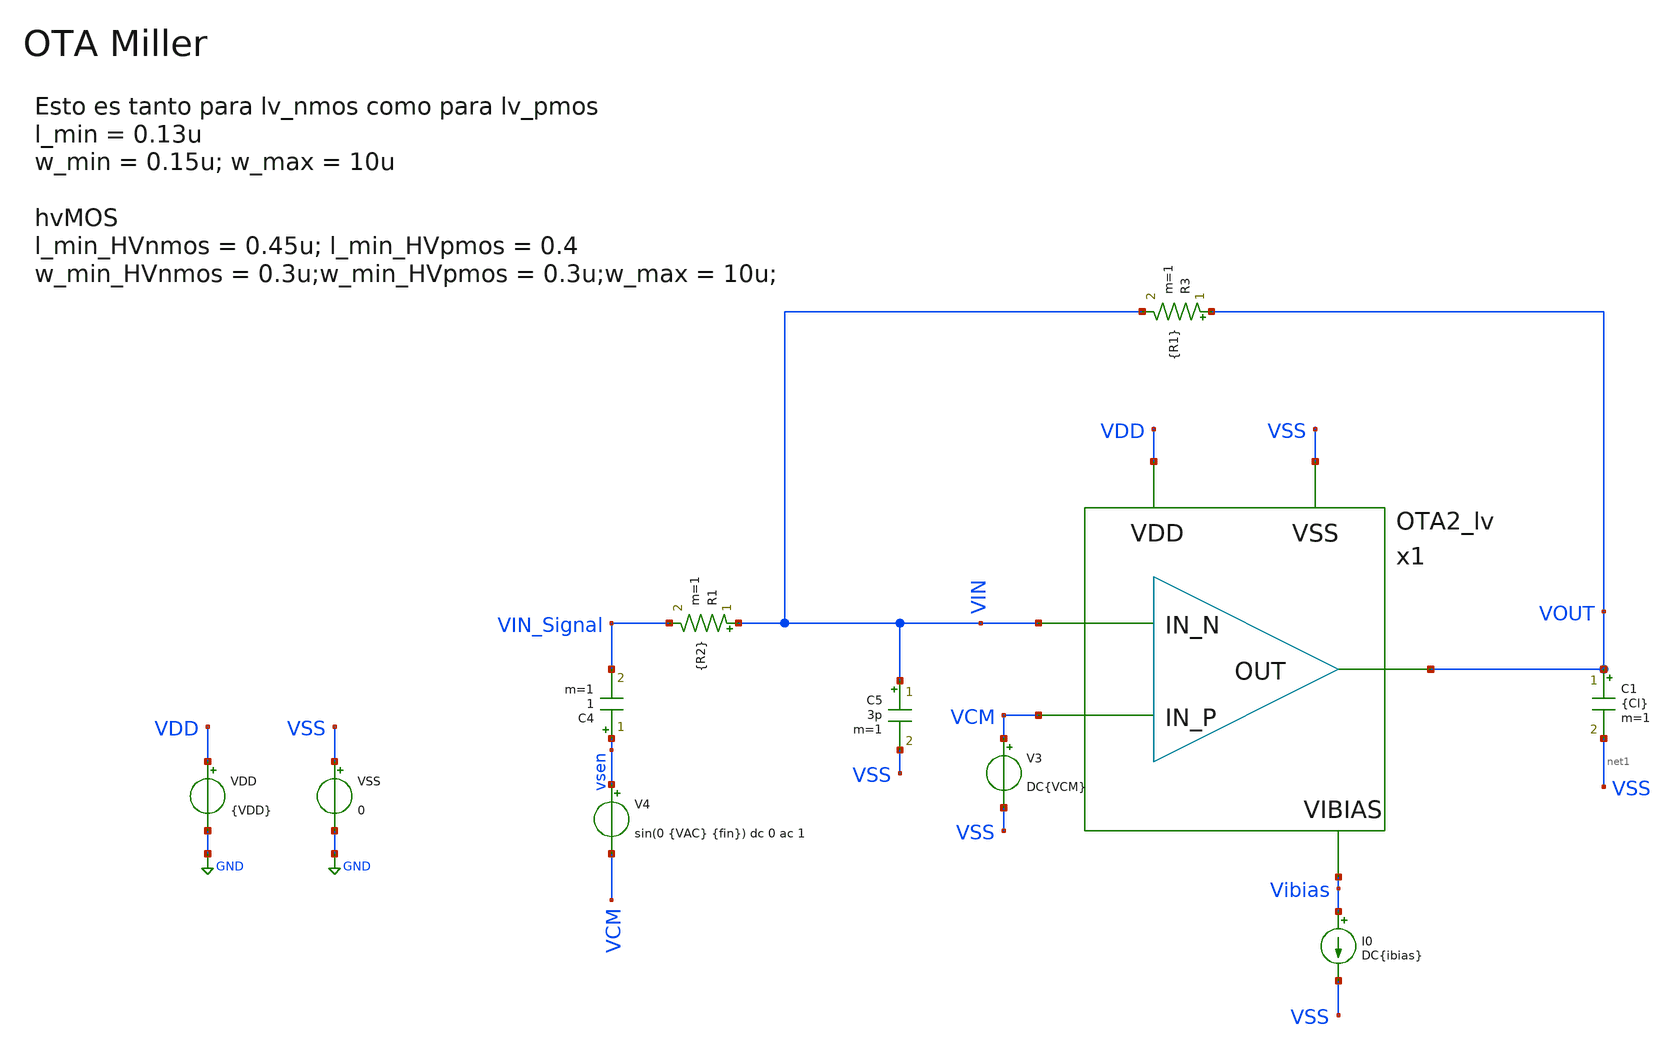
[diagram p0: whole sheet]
** sch_path: xschem/Ayudantias/Ayudantia_2/TB_OTA2_CL.sch
**.subckt TB_OTA2_CL
VDD VDD GND {VDD}
I0 Vibias VSS DC{ibias}
R3 VOUT VIN {R1} m=1
V3 VCM VSS DC{VCM}
VSS VSS GND 0
C5 VIN VSS 3p m=1
R1 VIN VIN_Signal {R2} m=1
C1 VOUT net1 {Cl} m=1
V4 vsen VCM sin(0 {VAC} {fin}) dc 0 ac 1
C4 vsen VIN_Signal 1 m=1
x1 VIN VCM VOUT VDD VSS Vibias OTA2_lv
**** begin user architecture code


*.param VDD = 3.3
.param VDD = 1.2
.param VCM = 0.6
.param Ibias = 100u
.param Pi = 3.14159265
.param fo = 60Meg
.param wo = 2*Pi*fo
.csparam wo = {wo}

.param VAC = 10m
*.param VAC  = 30m
*.param fin  = 9.765625e5
.param fin  = 0.8e5
.param T = 1/fin

.param R1 = 100k
*.param R2 = R1/10
.param R2 = R1/30

*.ic v(Vo) = 0

* OP Parameters & Singals to save
.save all

*.option temp = 125
*.option temp = -40
.option temp = 27





.lib cornerMOShv.lib mos_tt
.lib cornerMOSlv.lib mos_tt
*.lib cornerMOShv.lib mos_ff
*.lib cornerMOSlv.lib mos_ff
*.lib cornerMOShv.lib mos_ss
*.lib cornerMOSlv.lib mos_ss
*.lib cornerMOShv.lib mos_sf
*.lib cornerMOSlv.lib mos_sf
*.lib cornerMOShv.lib mos_fs
*.lib cornerMOSlv.lib mos_fs

.include /opt/pdks/ihp-sg13g2/libs.ref/sg13g2_stdcell/spice/sg13g2_stdcell.spice
.lib $::SG13G2_MODELS/cornerRES.lib res_typ
.lib $::SG13G2_MODELS/cornerCAP.lib cap_typ
*.lib $::SG13G2_MODELS/diodes.lib




*.param SimTime = 10*T
*.tran 0.01u {SimTime} uic
*.save all v(vsen)
.control
reset
  set color0 = white
  tran 0.01u 110u
  setplot tran1
  plot v(vsen) v(VOUT)
.endc

.end





.control
  set color0 = white
  *IPD413
 ac dec 200 1 1000Meg
 settype decibel VOUT
 *setplot ac1

 let phase_val = (180/PI)*cph(VOUT)
 *let phase_margin_val = 180 + 180/PI*cph(VOUT)
 let phase_margin_val = 360 + 180/PI*cph(VOUT)
 settype phase phase_val
 meas ac PM find phase_margin_val when vdb(VOUT)=0
 *meas ac PM find phase_val when vdb(VOUT)=0
 meas ac GM find vdb(vout) when vp(vout)=0
 *meas ac GM2 find vdb(vout) when vp(vout)=-180
 meas ac GBW WHEN vdb(VOUT)=0
 meas ac DCG find vdb(vout) at=1
 let DCG_BW = {DCG} - 3
 meas ac BW WHEN vdb(VOUT)={DCG_BW}

 let Av = 10^(DCG/20)
 print Av

 plot vdb(VOUT)
 plot phase_val
 plot phase_val vdb(VOUT)


 *wrdata /foss/designs/IPD413_2023_HW3_git/Data/data_phaseOTA1.dat phase_val
 *wrdata /foss/designs/IPD413_2023_HW3_git/Data/data_VdbOTA1.dat vdb(out)

 reset
  *DACI
  *ac dec 100 1 10G
  *setplot ac1
  *meas ac GBW when vdb(vout)=0
  *meas ac DCG find vdb(vout) at=1
  *meas ac PM find vp(vout) when vdb(vout)=0
  *print PM*180/PI
  *meas ac GM find vdb(vout) when vp(vout)=0

  *plot vdb(vout)
  *plot {vp(vout)*180/PI}
  *plot vdb(vout) {vp(vout)*180/PI}
.endc


.end





.param VDD = 1.2
.param VCM = 0.6

.control
reset
  op
  setplot op1
  unset filetype
  * VM1
  let VsdM1 = v(x1.VA) - v(x1.VB)
  let VsgM1 = v(x1.VA) - v(VCM)
  let VthM1 = @n.x1.xm1.nsg13_lv_pmos[vth]
  let VovM1 = VsgM1 - VthM1
  let gmM1 = @n.x1.xm1.nsg13_lv_pmos[gm]
  let gdsM1 = @n.x1.xm1.nsg13_lv_pmos[gds]
  let RoM1 = 1/gdsM1
  * VM2
  let VsdM2 = v(x1.VA) - v(x1.VC)
  let VsgM2 = v(x1.VA) - v(VIN)
  let VthM2 = @n.x1.xm2.nsg13_lv_pmos[vth]
  let VovM2 = VsgM2 - VthM2
  let gmM2 = @n.x1.xm2.nsg13_lv_pmos[gm]
  let gdsM2 = @n.x1.xm2.nsg13_lv_pmos[gds]
  let RoM2 = 1/gdsM2
  * VM3
  let VdsM3 = v(x1.VB) - v(VSS)
  let VthM3 = @n.x1.xm3.nsg13_lv_nmos[vth]
  let gmM3 = @n.x1.xm3.nsg13_lv_nmos[gm]
  let gdsM3 = @n.x1.xm3.nsg13_lv_nmos[gds]
  let RoM3 = 1/gdsM3
  * VM4
  let VdsM4 = v(x1.VC) - v(VSS)
  let VgsM4 = v(x1.VB) - v(VSS)
  let VthM4 = @n.x1.xm4.nsg13_lv_nmos[vth]
  let VovM4 = VgsM4 - VthM4
  let gmM4 = @n.x1.xm4.nsg13_lv_nmos[gm]
  let gdsM4 = @n.x1.xm4.nsg13_lv_nmos[gds]
  let RoM4 = 1/gdsM4
  * VM5
  let VsdM5 = v(VDD) - v(VOUT)
  let VsgM5 = v(VDD) - v(Vibias)
  let VthM5 = @n.x1.xm5.nsg13_lv_pmos[vth]
  let VovM5 = VsgM5 - VthM5
  let gmM5 = @n.x1.xm5.nsg13_lv_pmos[gm]
  let gdsM5 = @n.x1.xm5.nsg13_lv_pmos[gds]
  let RoM5 = 1/gdsM5
  * VM6
  let VdsM6 = v(VOUT) - v(VSS)
  let VgsM6 = v(x1.VC) - v(VSS)
  let VthM6 = @n.x1.xm6.nsg13_lv_nmos[vth]
  let VovM6 = VgsM6 - VthM6
  let gmM6 = @n.x1.xm6.nsg13_lv_nmos[gm]
  let gdsM6 = @n.x1.xm6.nsg13_lv_nmos[gds]
  let CggM6 = @n.x1.xm6.nsg13_lv_nmos[cgg]
  let RoM6 = 1/gdsM6
  * VM7
  let VsdM7 = v(VDD) - v(x1.VA)
  let VsgM7 = v(VDD) - v(Vibias)
  let VthM7 = @n.x1.xm7.nsg13_lv_pmos[vth]
  let VovM7 = VsgM7 - VthM7
  let gmM7 = @n.x1.xm7.nsg13_lv_pmos[gm]
  let gdsM7 = @n.x1.xm7.nsg13_lv_pmos[gds]
  let RoM7 = 1/gdsM7
  * VM8
  let VsdM8 = v(VDD) - v(Vibias)
  let VthM8 = @n.x1.xm8.nsg13_lv_pmos[vth]
  let VovM8 = VsdM8 - VthM8
  let gmM8 = @n.x1.xm8.nsg13_lv_pmos[gm]
  let gdsM8 = @n.x1.xm8.nsg13_lv_pmos[gds]
  let RoM8 = 1/gdsM8
  * VMR
  let VdsMR = v(x1.VC) - v(x1.VsMR)
  let gdsMR = @n.x1.xm9.nsg13_lv_nmos[gds]
  let RoMR = 1/gdsMR

  let Cc2 = gmM2/{wo}
  let Rc = 1/gmM6

  let Av1 = gmM1/(gdsM2+gdsM4)
  let Av2 = gmM6/(gdsM5+gdsM6)
  let Av = Av1*Av2
  let BW = (gdsM2+gdsM4)/(2*pi*Av2*{Cc})
  *let w1 = 1/((gdsM2+gdsM4)*gmM6*(gdsM6+gdsM7)*{Cc})
  *let w22 = gmM6/(CggM6+{Cl})
  let w2 = gmM6/(({Cl})*(1+CggM6/{Cc}))
  let GBW = gmM1/(2*pi*{Cc})
  *let GBW2 = gmM1/{Cc}
  let DCG = 20*log10(Av)
  *let fnd = gmM6/(2*pi*{Cl})

  print Av1 Av2 Av DCG
  print BW GBW w2
  print Rc Cc2

  write TB_OTA2_CL.raw
.endc

.end




.param temp=27

.param m_M8 = 500
.param m_M7 = 40
.param m_M5 = 11000
.param w_M8 =0.5u
.param w_M7 =0.5u
.param w_M5 =0.5u
.param l_M875 = 1u

.param m_M12 = 40
.param w_M12 =0.3u
.param l_M12 = 0.3u

.param m_M34 = 1
.param w_M34 =0.15u
.param l_M34 = 0.5u

.param m_M6 = 10
.param w_M6 =10u
.param l_M6 = 0.13u

.param m_R = 1
.param w_R =0.15u
.param l_R = 0.13u

.param Cc = 0.1p
.param Cl = 20p
.csparam Cl = {Cl}
.csparam Cc = {Cc}






**** end user architecture code
**.ends

* expanding   symbol:
*+  /workspaces/usm-vlsi-tools/shared_xserver/simulations/Projects/IHP/IPD413_202501/xschem/Tareas/Tarea_2/OTA2_lv.sym # of pins=6
** sym_path: xschem/Ayudantias/Ayudantia_2/OTA2_lv.sym
** sch_path: xschem/Ayudantias/Ayudantia_2/OTA2_lv.sch
.subckt OTA2_lv IN_N IN_P OUT VDD VSS Vibias
*.ipin IN_N
*.ipin IN_P
*.ipin Vibias
*.opin OUT
*.iopin VDD
*.iopin VSS
XM1 VB IN_N net1 VA sg13_lv_pmos w={w_M12} l={l_M12} ng=1 m={m_M12} mm_ok=1
XM3 VSS VB VB VSS sg13_lv_nmos w={w_M34} l={l_M34} ng=1 m={m_M34} mm_ok=1
XM2 VC IN_P net2 VA sg13_lv_pmos w={w_M12} l={l_M12} ng=1 m={m_M12} mm_ok=1
XM4 VSS VB net6 VSS sg13_lv_nmos w={w_M34} l={l_M34} ng=1 m={m_M34} mm_ok=1
XM5 net5 Vibias VDD VDD sg13_lv_pmos w={w_M5} l={l_M875} ng=1 m={m_M5} mm_ok=1
XM6 VSS VC net3 VSS sg13_lv_nmos w={w_M6} l={l_M6} ng=1 m={m_M6} mm_ok=1
XM7 net7 Vibias VDD VDD sg13_lv_pmos w={w_M7} l={l_M875} ng=1 m={m_M7} mm_ok=1
XM8 net8 Vibias VDD VDD sg13_lv_pmos w={w_M8} l={l_M875} ng=1 m={m_M8} mm_ok=1
XM9 VsMR VDD VC VSS sg13_lv_nmos w={w_R} l={l_R} ng=1 m={m_R} mm_ok=1
C1 VsMR net4 {Cc} m=1
Vmeas VA net1 0
.save i(vmeas)
Vmeas1 VC net6 0
.save i(vmeas1)
Vmeas2 VA net2 0
.save i(vmeas2)
Vmeas3 net4 net3 0
.save i(vmeas3)
Vmeas4 net5 net4 0
.save i(vmeas4)
Vmeas5 net7 VA 0
.save i(vmeas5)
Vmeas6 net8 Vibias 0
.save i(vmeas6)
Vmeas7 net4 OUT 0
.save i(vmeas7)
.ends

.GLOBAL GND
.end
